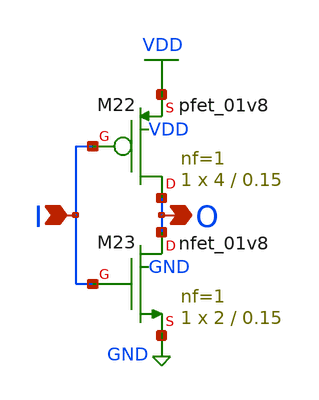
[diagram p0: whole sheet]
** sch_path: lib/pdk_examples/inverter.sch
**.subckt inverter I O
*.ipin I
*.opin O
XM22 O I VDD VDD sky130_fd_pr__pfet_01v8 L=0.15 W=4 nf=1 ad='int((nf+1)/2) * W/nf * 0.29' as='int((nf+2)/2) * W/nf * 0.29'
+ pd='2*int((nf+1)/2) * (W/nf + 0.29)' ps='2*int((nf+2)/2) * (W/nf + 0.29)' nrd='0.29 / W' nrs='0.29 / W'
+ sa=0 sb=0 sd=0 mult=1 m=1
XM23 O I GND GND sky130_fd_pr__nfet_01v8 L=0.15 W=2 nf=1 ad='int((nf+1)/2) * W/nf * 0.29' as='int((nf+2)/2) * W/nf * 0.29'
+ pd='2*int((nf+1)/2) * (W/nf + 0.29)' ps='2*int((nf+2)/2) * (W/nf + 0.29)' nrd='0.29 / W' nrs='0.29 / W'
+ sa=0 sb=0 sd=0 mult=1 m=1
**.ends
.GLOBAL VDD
.GLOBAL GND
.end
